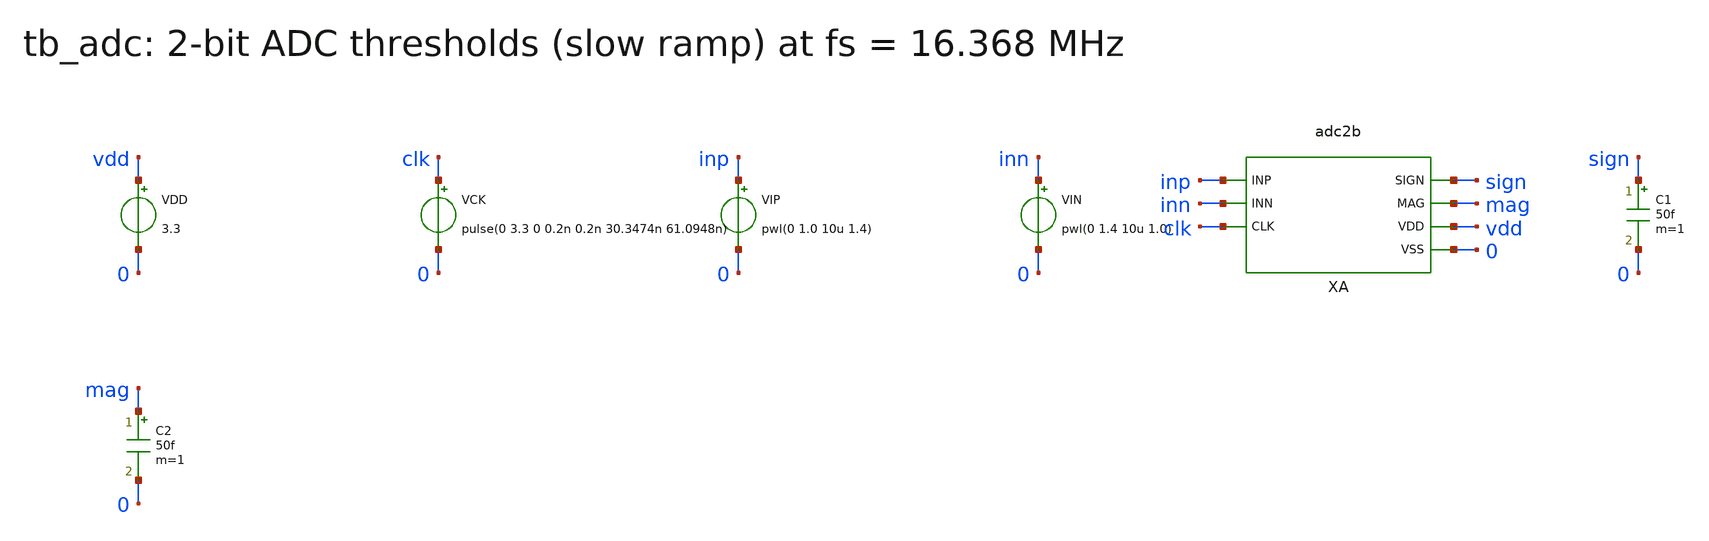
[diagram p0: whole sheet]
** sch_path: v1_claude/xschem/tb_adc.sch
**.subckt tb_adc
VDD vdd 0 3.3
VCK clk 0 pulse(0 3.3 0 0.2n 0.2n 30.3474n 61.0948n)
VIP inp 0 pwl(0 1.0 10u 1.4)
VIN inn 0 pwl(0 1.4 10u 1.0)
XA inp inn clk sign mag vdd 0 adc2b
C1 sign 0 50f m=1
C2 mag 0 50f m=1
**** begin user architecture code
 .include $::180MCU_MODELS/design.ngspice
.lib $::180MCU_MODELS/sm141064.ngspice typical
.lib $::180MCU_MODELS/sm141064.ngspice res_typical
.lib $::180MCU_MODELS/sm141064.ngspice mimcap_typical

.control
set num_threads=1
tran 0.1n 10u
let vd = v(inp)-v(inn)
meas tran ts when v(sign)=1.65 rise=1
meas tran tm1 when v(mag)=1.65 fall=1
meas tran tm2 when v(mag)=1.65 rise=1
meas tran vs find vd at=ts
meas tran vm1 find vd at=tm1
meas tran vm2 find vd at=tm2
echo RES vth_sign=$&vs vth_mag_lo=$&vm1 vth_mag_hi=$&vm2
meas tran thp avg v(xa.thp) from=2u to=8u
meas tran thm avg v(xa.thm) from=2u to=8u
meas tran thn avg v(xa.thn) from=2u to=8u
echo RES ladder thp=$&thp thm=$&thm thn=$&thn
meas tran iavg avg i(VDD) from=2u to=8u
echo RES iavg=$&iavg
.endc

**** end user architecture code
**.ends
.end
